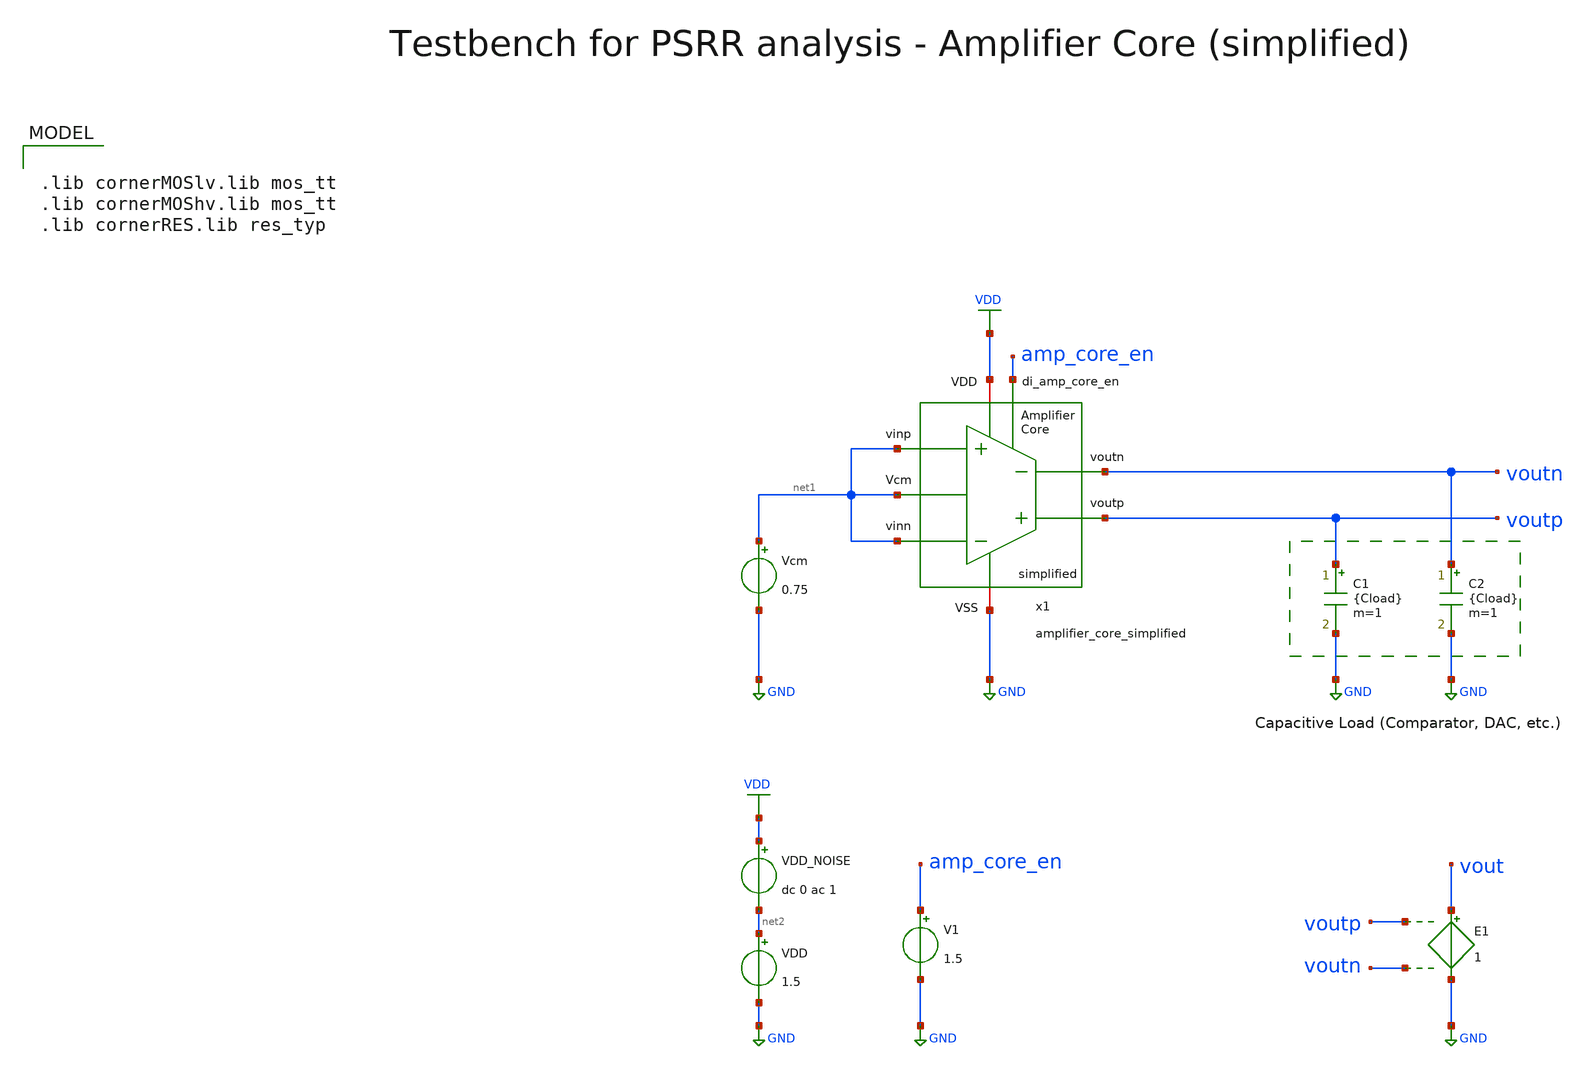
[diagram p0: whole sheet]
** sch_path: SG13G2_ATBS-ADC-main/xschem/bio_amplifier/amplifier_core/testbenches/amplifier_core_simplified_tb_PSRR.sch
**.subckt amplifier_core_simplified_tb_PSRR
C1 voutp GND {Cload} m=1
C2 voutn GND {Cload} m=1
Vcm net1 GND 0.75
V1 amp_core_en GND 1.5
E1 vout GND voutp voutn 1
x1 voutp voutn amp_core_en net1 net1 VDD GND net1 amplifier_core_simplified
VDD net2 GND 1.5
VDD_NOISE VDD net2 dc 0 ac 1
**** begin user architecture code


.param temp=27
* 228fF DAC + (1 - beta) * 3.3pF
.param Cload=3.49p
.options savecurrents method=gear reltol=1e-2 abstol=1e-15 gmin=1e-15 rshunt=1e15
.control

save v(VDD) v(vout) v(voutp) v(voutn)

set wr_vecnames
set wr_singlescale

* User Constants
let f_min = 10m
let f_max = 1G
let fdc = 1

* Operating Point Analysis
op
remzerovec
write amplifier_core_simplified_tb_PSRR.raw
set appendwrite

* AC Analysis
ac dec 101 $&const.f_min $&const.f_max
remzerovec
write amplifier_core_simplified_tb_PSRR.raw

* Plotting
let PSRR = v(VDD)/v(vout)
let PSRRp = v(VDD)/v(voutp)
let PSRRn = v(VDD)/v(voutn)

let PSRR_dB = vdb(PSRR)
let PSRRp_dB = vdb(PSRRp)
let PSRRn_dB = vdb(PSRRn)

plot PSRR_dB PSRRp_dB PSRRn_dB ylabel 'PSRR, PSRR+, PSRR-'

* Measurements
meas ac PSRRdc_dB find PSRR_dB when frequency = fdc
print PSRRdc_dB

meas ac PSRRpdc_dB find PSRRp_dB when frequency = fdc
print PSRRpdc_dB

meas ac PSRRndc_dB find PSRRn_dB when frequency = fdc
print PSRRndc_dB

* Write Data
set wr_vecnames
set wr_singlescale
wrdata
+ /foss/designs/SG13G2_ATBS-ADC-main/python/plot_simulations/data/amplifier_core_simplified_tb_PSRR.txt v(PSRR_dB)

*quit
.endc



.lib cornerMOSlv.lib mos_tt
.lib cornerMOShv.lib mos_tt
.lib cornerRES.lib res_typ

**** end user architecture code
**.ends
.GLOBAL GND
.GLOBAL VDD
.end
